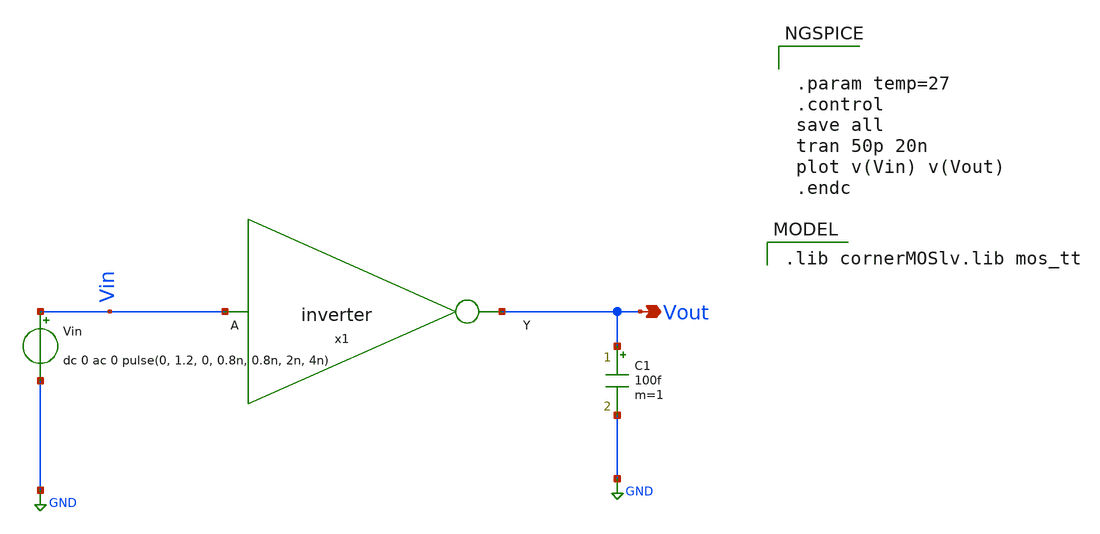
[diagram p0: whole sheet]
** sch_path: Type-II PLL-based Clock Multiplier in 130nm Bi-CMOS Technology/xschem/Inverter/inverter_tb.sch
**.subckt inverter_tb Vout
*.opin Vout
Vin Vin GND dc 0 ac 0 pulse(0, 1.2, 0, 0.8n, 0.8n, 2n, 4n)
C1 Vout GND 100f m=1
x1 Vout Vin inverter
**** begin user architecture code
 .lib cornerMOSlv.lib mos_tt



.param temp=27
.control
save all
tran 50p 20n
plot v(Vin) v(Vout)
.endc


**** end user architecture code
**.ends
.GLOBAL GND
.end
